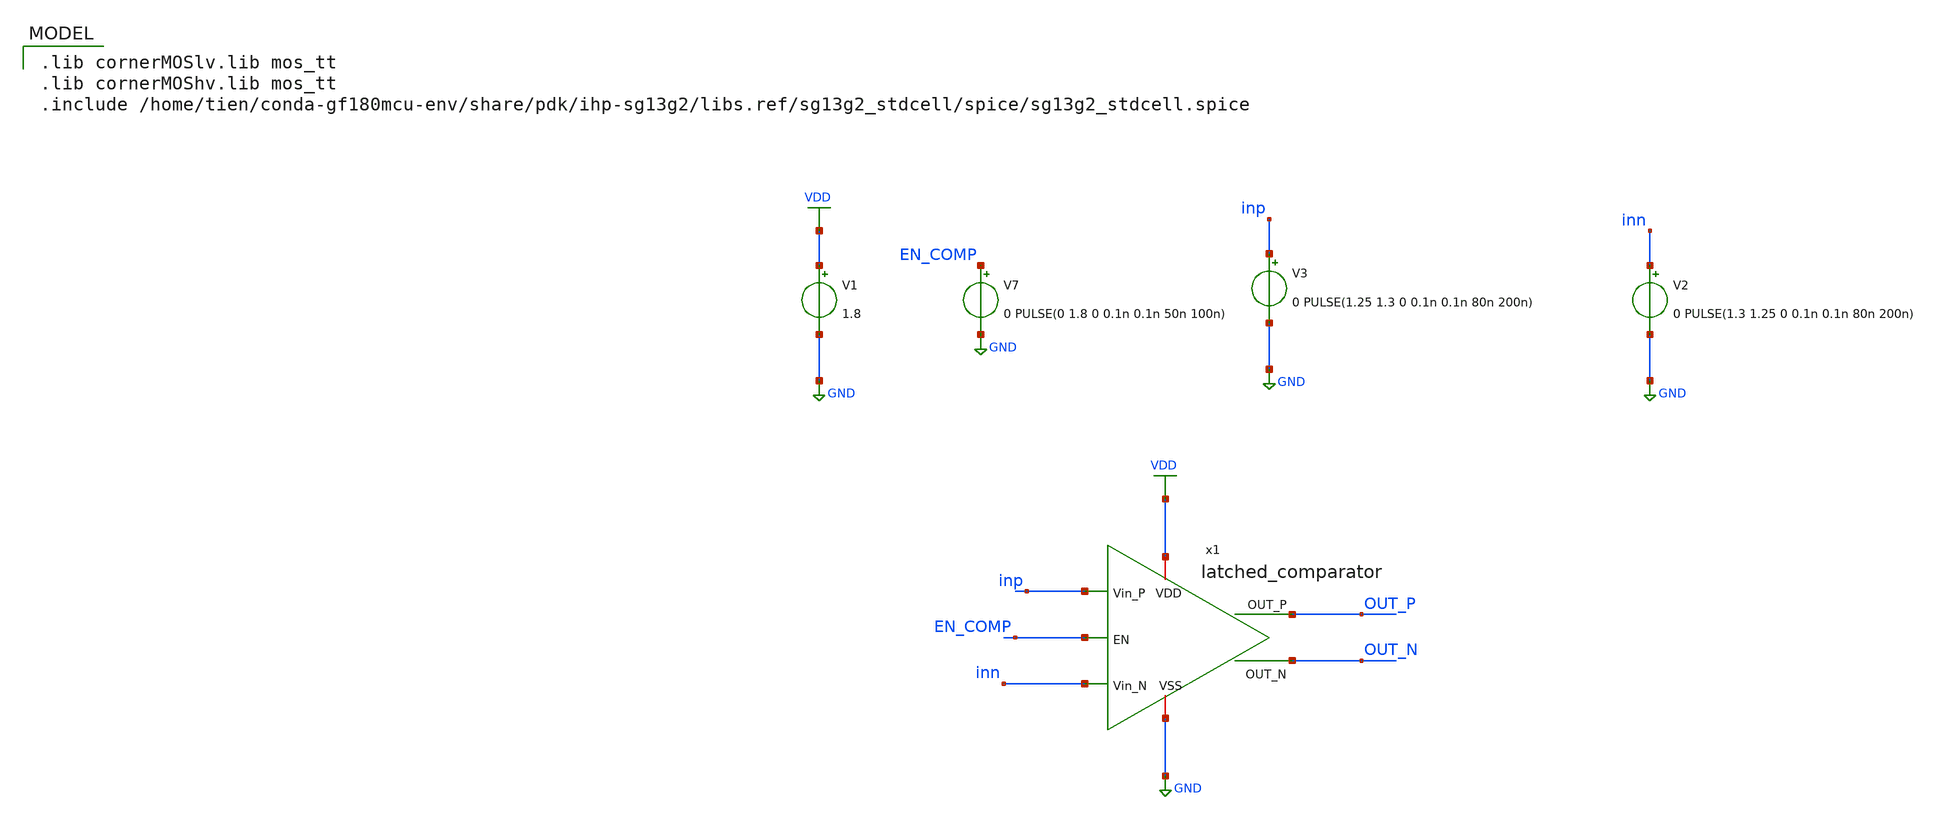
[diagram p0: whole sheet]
** sch_path: schematic/simulations/latched_comparator_tb.sch
* IHP-GmbH/IHP-Open-PDK/ihp-sg13g2/libs.tech/xschem/sg13g2_stdcells/sg13g2_buf_4.sch:
* Copyright 2023 IHP PDK Authors
* Licensed under the Apache License, Version 2.0 (the "License");
**.subckt latched_comparator_tb
x1 VDD inp inn OUT_P EN_COMP OUT_N GND latched_comparator
V1 VDD GND 1.8
V3 inp GND 0 PULSE(1.25 1.3 0 0.1n 0.1n 80n 200n)
V2 inn GND 0 PULSE(1.3 1.25 0 0.1n 0.1n 80n 200n)
V7 EN_COMP GND 0 PULSE(0 1.8 0 0.1n 0.1n 50n 100n)
.save i(v7)
**** begin user architecture code
 .lib cornerMOSlv.lib mos_tt
.lib cornerMOShv.lib mos_tt
.include /home/tien/conda-gf180mcu-env/share/pdk/ihp-sg13g2/libs.ref/sg13g2_stdcell/spice/sg13g2_stdcell.spice




.option temp = 27
.save all

.option GMIN=1e-12 reltol=1e-6

.tran 10n 100u


**** end user architecture code
**.ends

* expanding   symbol:  latched_comparator/latched_comparator.sym # of pins=7
** sym_path: schematic/latched_comparator/latched_comparator.sym
** sch_path: schematic/latched_comparator/latched_comparator.sch
.subckt latched_comparator VDD Vin_P Vin_N OUT_P EN OUT_N VSS
*.ipin Vin_P
*.ipin Vin_N
*.iopin VDD
*.iopin VSS
*.ipin EN
*.opin OUT_P
*.opin OUT_N
XM1 net1 ENi VDD VDD sg13_lv_pmos w=0.32u l=0.15u ng=1 m=1 mm_ok=1
XM2 OUT_Ni ENi VDD VDD sg13_lv_pmos w=0.32u l=0.15u ng=1 m=1 mm_ok=1
XM3 OUT_Ni OUT_Pi VDD VDD sg13_lv_pmos w=1.25u l=0.15u ng=1 m=1 mm_ok=1
XM4 net2 ENi VDD VDD sg13_lv_pmos w=0.32u l=0.15u ng=1 m=1 mm_ok=1
XM5 OUT_Pi ENi VDD VDD sg13_lv_pmos w=0.32u l=0.15u ng=1 m=1 mm_ok=1
XM6 OUT_Pi OUT_Ni VDD VDD sg13_lv_pmos w=1.25u l=0.15u ng=1 m=1 mm_ok=1
XM7 net1 Vin_P net3 VSS sg13_lv_nmos w=0.55u l=0.13u ng=1 m=1 mm_ok=1
XM8 net2 Vin_N net3 VSS sg13_lv_nmos w=0.55u l=0.13u ng=1 m=1 mm_ok=1
XM9 OUT_Pi OUT_Ni net2 VSS sg13_lv_nmos w=0.42u l=0.15u ng=1 m=1 mm_ok=1
XM10 OUT_Ni OUT_Pi net1 VSS sg13_lv_nmos w=0.42u l=0.15u ng=1 m=1 mm_ok=1
XM11 net3 net3 net3 VSS sg13_lv_nmos w=0.55u l=0.13u ng=1 m=2 mm_ok=1
XM12 net3 ENi VSS VSS sg13_lv_nmos w=0.9u l=0.15u ng=1 m=2 mm_ok=1
x4 net4 OUT_Pi VDD VSS sg13g2_inv_2
x5 net5 OUT_Ni VDD VSS sg13g2_inv_2
x1 ENi EN VDD VSS sg13g2_buf_4
x6 OUT_P net4 VDD VSS sg13g2_inv_4
x2 OUT_N net5 VDD VSS sg13g2_inv_4
.ends


* expanding   symbol:  sg13g2_stdcells/sg13g2_inv_2.sym # of pins=2
** sym_path: sg13g2_stdcells/sg13g2_inv_2.sym
** sch_path: sg13g2_stdcells/sg13g2_inv_2.sch
.subckt sg13g2_inv_2 Y A VDD VSS
*.opin Y
*.ipin A
*.iopin VDD
*.iopin VSS
XM1 Y A VSS VSS sg13_lv_nmos w=1.48u l=130.00n ng=2 m=1 mm_ok=1
XM2 Y A VDD VDD sg13_lv_pmos w=2.24u l=130.00n ng=2 m=1 mm_ok=1
.ends


* expanding   symbol:  sg13g2_stdcells/sg13g2_buf_4.sym # of pins=2
** sym_path: sg13g2_stdcells/sg13g2_buf_4.sym
** sch_path: sg13g2_stdcells/sg13g2_buf_4.sch
.subckt sg13g2_buf_4 X A VDD VSS
*.ipin A
*.opin X
*.iopin VDD
*.iopin VSS
XM1 net1 A VSS VSS sg13_lv_nmos w=740.00n l=130.00n ng=1 m=1 mm_ok=1
XM2 X net1 VSS VSS sg13_lv_nmos w=2.96u l=130.00n ng=4 m=1 mm_ok=1
XM3 net1 A VDD VDD sg13_lv_pmos w=1.68u l=130.00n ng=2 m=1 mm_ok=1
XM4 X net1 VDD VDD sg13_lv_pmos w=4.48u l=130.00n ng=4 m=1 mm_ok=1
.ends


* expanding   symbol:  sg13g2_stdcells/sg13g2_inv_4.sym # of pins=2
** sym_path: sg13g2_stdcells/sg13g2_inv_4.sym
** sch_path: sg13g2_stdcells/sg13g2_inv_4.sch
.subckt sg13g2_inv_4 Y A VDD VSS
*.ipin A
*.opin Y
*.iopin VDD
*.iopin VSS
XM1 Y A VSS VSS sg13_lv_nmos w=2.96u l=130.00n ng=4 m=1 mm_ok=1
XM2 Y A VDD VDD sg13_lv_pmos w=4.48u l=130.00n ng=4 m=1 mm_ok=1
.ends

.GLOBAL GND
.GLOBAL VDD
.end
